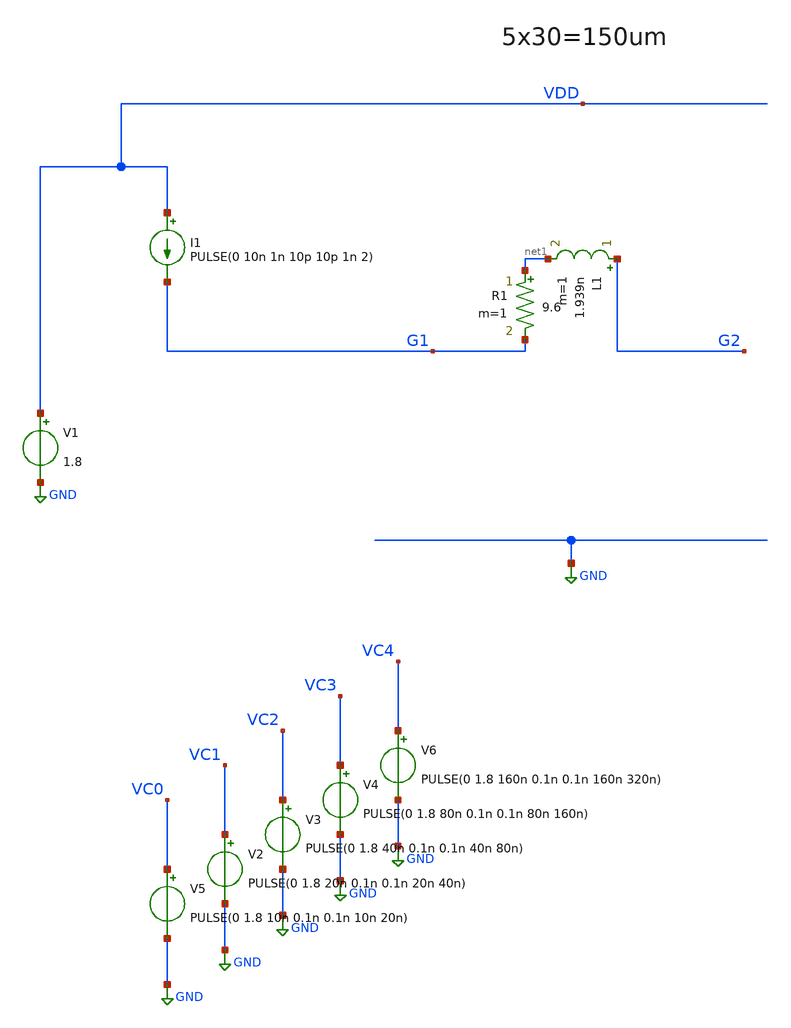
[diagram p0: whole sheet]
** sch_path: xschem/OSC_LF1_PEX.sch
**.subckt OSC_LF1_PEX
V1 VDD GND 1.8
I1 VDD G1 PULSE(0 10n 1n 10p 10p 1n 2)
L1 G2 net1 1.939n m=1
V5 VC0 GND PULSE(0 1.8 10n 0.1n 0.1n 10n 20n)
V2 VC1 GND PULSE(0 1.8 20n 0.1n 0.1n 20n 40n)
V3 VC2 GND PULSE(0 1.8 40n 0.1n 0.1n 40n 80n)
V4 VC3 GND PULSE(0 1.8 80n 0.1n 0.1n 80n 160n)
V6 VC4 GND PULSE(0 1.8 160n 0.1n 0.1n 160n 320n)
R1 net1 G1 9.6 m=1
**** begin user architecture code
.lib $::SKYWATER_MODELS/sky130.lib.spice ff
* .include $::PDKPATH/libs.ref/sky130_fd_sc_hvl/spice/sky130_fd_sc_hvl.spice



* .subckt sky130_fd_pr__rf_nfet_01v8_bM04W5p00L0p15_ext DRAIN GATE SOURCE SUBSTRATE
* X0 DRAIN GATE SOURCE SUBSTRATE sky130_fd_pr__nfet_01v8 ad=2.828e+12p pd=2.132e+07u as=4.242e+12p
*+ ps=3.198e+07u w=5.05e+06u l=150000u
* X1 SOURCE SUBSTRATE SUBSTRATE SUBSTRATE sky130_fd_pr__nfet_01v8 ad=0p pd=0u as=3.03e+12p
*+ ps=2.14e+07u w=5.05e+06u l=150000u
* X2 SOURCE GATE DRAIN SUBSTRATE sky130_fd_pr__nfet_01v8 ad=0p pd=0u as=0p ps=0u w=5.05e+06u
*+ l=150000u
* X3 DRAIN GATE SOURCE SUBSTRATE sky130_fd_pr__nfet_01v8 ad=0p pd=0u as=0p ps=0u w=5.05e+06u
*+ l=150000u
* X4 SUBSTRATE SUBSTRATE SOURCE SUBSTRATE sky130_fd_pr__nfet_01v8 ad=0p pd=0u as=0p ps=0u
*+ w=5.05e+06u l=150000u
* X5 SOURCE GATE DRAIN SUBSTRATE sky130_fd_pr__nfet_01v8 ad=0p pd=0u as=0p ps=0u w=5.05e+06u
*+ l=150000u
* .ends

**** CROSS COUPLED PAIRS ****

.subckt XCP VH VL G1 G2

.subckt sky130_fd_pr__rf_pfet_01v8_aF04W5p00L0p15 DRAIN GATE SOURCE
X0 DRAIN GATE SOURCE SOURCE sky130_fd_pr__pfet_01v8 ad=2.8e+12p pd=2.112e+07u as=4.05e+12p
+ ps=3.162e+07u w=5e+06u l=150000u
X1 SOURCE GATE DRAIN SOURCE sky130_fd_pr__pfet_01v8 ad=0p pd=0u as=0p ps=0u w=5e+06u l=150000u
X2 SOURCE GATE DRAIN SOURCE sky130_fd_pr__pfet_01v8 ad=0p pd=0u as=0p ps=0u w=5e+06u l=150000u
X3 DRAIN GATE SOURCE SOURCE sky130_fd_pr__pfet_01v8 ad=0p pd=0u as=0p ps=0u w=5e+06u l=150000u
C0 DRAIN SOURCE 6.07fF
.ends



X0 VL G1 G2 VL sky130_fd_pr__nfet_01v8 ad=0p pd=0u as=0p ps=0u w=5.05e+06u l=150000u
X1 VL G1 G2 VL sky130_fd_pr__nfet_01v8 ad=0p pd=0u as=0p ps=0u w=5.05e+06u l=150000u
X2 G2 G1 VL VL sky130_fd_pr__nfet_01v8 ad=0p pd=0u as=0p ps=0u w=5.05e+06u l=150000u
X3 G2 G1 VL VL sky130_fd_pr__nfet_01v8 ad=0p pd=0u as=0p ps=0u w=5.05e+06u l=150000u
X4 VL G1 G2 VL sky130_fd_pr__nfet_01v8 ad=0p pd=0u as=0p ps=0u w=5.05e+06u l=150000u
X5 VL G1 G2 VL sky130_fd_pr__nfet_01v8 ad=0p pd=0u as=0p ps=0u w=5.05e+06u l=150000u
X6 G2 G1 VL VL sky130_fd_pr__nfet_01v8 ad=0p pd=0u as=0p ps=0u w=5.05e+06u l=150000u
X7 G2 G1 VL VL sky130_fd_pr__nfet_01v8 ad=0p pd=0u as=0p ps=0u w=5.05e+06u l=150000u
X8 VL G1 G2 VL sky130_fd_pr__nfet_01v8 ad=0p pd=0u as=0p ps=0u w=5.05e+06u l=150000u
X9 VL G1 G2 VL sky130_fd_pr__nfet_01v8 ad=0p pd=0u as=0p ps=0u w=5.05e+06u l=150000u
X10 G2 G1 VL VL sky130_fd_pr__nfet_01v8 ad=0p pd=0u as=0p ps=0u w=5.05e+06u l=150000u
X11 G2 G1 VL VL sky130_fd_pr__nfet_01v8 ad=0p pd=0u as=0p ps=0u w=5.05e+06u l=150000u
X12 VL G2 G1 VL sky130_fd_pr__nfet_01v8 ad=0p pd=0u as=0p ps=0u w=5.05e+06u l=150000u
X13 VL G2 G1 VL sky130_fd_pr__nfet_01v8 ad=0p pd=0u as=0p ps=0u w=5.05e+06u l=150000u
X14 G1 G2 VL VL sky130_fd_pr__nfet_01v8 ad=0p pd=0u as=0p ps=0u w=5.05e+06u l=150000u
X15 G1 G2 VL VL sky130_fd_pr__nfet_01v8 ad=0p pd=0u as=0p ps=0u w=5.05e+06u l=150000u
X16 VL G2 G1 VL sky130_fd_pr__nfet_01v8 ad=0p pd=0u as=0p ps=0u w=5.05e+06u l=150000u
X17 VL G2 G1 VL sky130_fd_pr__nfet_01v8 ad=0p pd=0u as=0p ps=0u w=5.05e+06u l=150000u
X18 G1 G2 VL VL sky130_fd_pr__nfet_01v8 ad=0p pd=0u as=0p ps=0u w=5.05e+06u l=150000u
X19 G1 G2 VL VL sky130_fd_pr__nfet_01v8 ad=0p pd=0u as=0p ps=0u w=5.05e+06u l=150000u
X20 VL G2 G1 VL sky130_fd_pr__nfet_01v8 ad=0p pd=0u as=0p ps=0u w=5.05e+06u l=150000u
X21 VL G2 G1 VL sky130_fd_pr__nfet_01v8 ad=0p pd=0u as=0p ps=0u w=5.05e+06u l=150000u
X22 G1 G2 VL VL sky130_fd_pr__nfet_01v8 ad=0p pd=0u as=0p ps=0u w=5.05e+06u l=150000u
X23 G1 G2 VL VL sky130_fd_pr__nfet_01v8 ad=0p pd=0u as=0p ps=0u w=5.05e+06u l=150000u
C0 G1 VH 48.54fF
C1 VH G2 48.59fF
C2 G1 G2 16.60fF
XRF_pfet_28xW5p0L0p15_0/sky130_fd_pr__rf_pfet_01v8_aF04W5p00L0p15_0 G2 G1 VH
+ sky130_fd_pr__rf_pfet_01v8_aF04W5p00L0p15
XRF_pfet_28xW5p0L0p15_0/sky130_fd_pr__rf_pfet_01v8_aF04W5p00L0p15_1 G2 G1 VH
+ sky130_fd_pr__rf_pfet_01v8_aF04W5p00L0p15
XRF_pfet_28xW5p0L0p15_0/sky130_fd_pr__rf_pfet_01v8_aF04W5p00L0p15_2 G2 G1 VH
+ sky130_fd_pr__rf_pfet_01v8_aF04W5p00L0p15
XRF_pfet_28xW5p0L0p15_0/sky130_fd_pr__rf_pfet_01v8_aF04W5p00L0p15_3 G2 G1 VH
+ sky130_fd_pr__rf_pfet_01v8_aF04W5p00L0p15
XRF_pfet_28xW5p0L0p15_0/sky130_fd_pr__rf_pfet_01v8_aF04W5p00L0p15_4 G2 G1 VH
+ sky130_fd_pr__rf_pfet_01v8_aF04W5p00L0p15
XRF_pfet_28xW5p0L0p15_0/sky130_fd_pr__rf_pfet_01v8_aF04W5p00L0p15_5 G2 G1 VH
+ sky130_fd_pr__rf_pfet_01v8_aF04W5p00L0p15
XRF_pfet_28xW5p0L0p15_0/sky130_fd_pr__rf_pfet_01v8_aF04W5p00L0p15_6 G2 G1 VH
+ sky130_fd_pr__rf_pfet_01v8_aF04W5p00L0p15
XRF_pfet_28xW5p0L0p15_1/sky130_fd_pr__rf_pfet_01v8_aF04W5p00L0p15_0 G1 G2 VH
+ sky130_fd_pr__rf_pfet_01v8_aF04W5p00L0p15
XRF_pfet_28xW5p0L0p15_1/sky130_fd_pr__rf_pfet_01v8_aF04W5p00L0p15_1 G1 G2 VH
+ sky130_fd_pr__rf_pfet_01v8_aF04W5p00L0p15
XRF_pfet_28xW5p0L0p15_1/sky130_fd_pr__rf_pfet_01v8_aF04W5p00L0p15_2 G1 G2 VH
+ sky130_fd_pr__rf_pfet_01v8_aF04W5p00L0p15
XRF_pfet_28xW5p0L0p15_1/sky130_fd_pr__rf_pfet_01v8_aF04W5p00L0p15_3 G1 G2 VH
+ sky130_fd_pr__rf_pfet_01v8_aF04W5p00L0p15
XRF_pfet_28xW5p0L0p15_1/sky130_fd_pr__rf_pfet_01v8_aF04W5p00L0p15_4 G1 G2 VH
+ sky130_fd_pr__rf_pfet_01v8_aF04W5p00L0p15
XRF_pfet_28xW5p0L0p15_1/sky130_fd_pr__rf_pfet_01v8_aF04W5p00L0p15_5 G1 G2 VH
+ sky130_fd_pr__rf_pfet_01v8_aF04W5p00L0p15
XRF_pfet_28xW5p0L0p15_1/sky130_fd_pr__rf_pfet_01v8_aF04W5p00L0p15_6 G1 G2 VH
+ sky130_fd_pr__rf_pfet_01v8_aF04W5p00L0p15
C3 G1 VL 22.49fF
C4 G2 VL 22.37fF
C5 VH VL 25.01fF
.ends


**** CAPTUNE ****

.subckt CAPTUNE TOP BOT SUB G0 G1 G2 G3 G4

X0 BOT G0 sky130_fd_pr__rf_nfet_01v8_aM04W5p00L0p15_fingered_0/S SUB sky130_fd_pr__nfet_01v8 ad=0p
+ pd=0u as=0p ps=0u w=5.05e+06u l=150000u
X1 BOT G0 sky130_fd_pr__rf_nfet_01v8_aM04W5p00L0p15_fingered_0/S SUB sky130_fd_pr__nfet_01v8 ad=0p
+ pd=0u as=0p ps=0u w=5.05e+06u l=150000u
X2 sky130_fd_pr__rf_nfet_01v8_aM04W5p00L0p15_fingered_0/S G0 BOT SUB sky130_fd_pr__nfet_01v8 ad=0p
+ pd=0u as=0p ps=0u w=5.05e+06u l=150000u
X3 sky130_fd_pr__rf_nfet_01v8_aM04W5p00L0p15_fingered_0/S G0 BOT SUB sky130_fd_pr__nfet_01v8 ad=0p
+ pd=0u as=0p ps=0u w=5.05e+06u l=150000u
X4 BOT G1 sky130_fd_pr__rf_nfet_01v8_aM04W5p00L0p15_fingered_1/S SUB sky130_fd_pr__nfet_01v8 ad=0p
+ pd=0u as=0p ps=0u w=5.05e+06u l=150000u
X5 BOT G1 sky130_fd_pr__rf_nfet_01v8_aM04W5p00L0p15_fingered_1/S SUB sky130_fd_pr__nfet_01v8 ad=0p
+ pd=0u as=0p ps=0u w=5.05e+06u l=150000u
X6 sky130_fd_pr__rf_nfet_01v8_aM04W5p00L0p15_fingered_1/S G1 BOT SUB sky130_fd_pr__nfet_01v8 ad=0p
+ pd=0u as=0p ps=0u w=5.05e+06u l=150000u
X7 sky130_fd_pr__rf_nfet_01v8_aM04W5p00L0p15_fingered_1/S G1 BOT SUB sky130_fd_pr__nfet_01v8 ad=0p
+ pd=0u as=0p ps=0u w=5.05e+06u l=150000u
X8 BOT G2 sky130_fd_pr__rf_nfet_01v8_aM04W5p00L0p15_fingered_2/S SUB sky130_fd_pr__nfet_01v8 ad=0p
+ pd=0u as=0p ps=0u w=5.05e+06u l=150000u
X9 BOT G2 sky130_fd_pr__rf_nfet_01v8_aM04W5p00L0p15_fingered_2/S SUB sky130_fd_pr__nfet_01v8 ad=0p
+ pd=0u as=0p ps=0u w=5.05e+06u l=150000u
X10 sky130_fd_pr__rf_nfet_01v8_aM04W5p00L0p15_fingered_2/S G2 BOT SUB sky130_fd_pr__nfet_01v8 ad=0p
+ pd=0u as=0p ps=0u w=5.05e+06u l=150000u
X11 sky130_fd_pr__rf_nfet_01v8_aM04W5p00L0p15_fingered_2/S G2 BOT SUB sky130_fd_pr__nfet_01v8 ad=0p
+ pd=0u as=0p ps=0u w=5.05e+06u l=150000u
X12 BOT G3 sky130_fd_pr__rf_nfet_01v8_aM04W5p00L0p15_fingered_4/S SUB sky130_fd_pr__nfet_01v8 ad=0p
+ pd=0u as=0p ps=0u w=5.05e+06u l=150000u
X13 BOT G3 sky130_fd_pr__rf_nfet_01v8_aM04W5p00L0p15_fingered_4/S SUB sky130_fd_pr__nfet_01v8 ad=0p
+ pd=0u as=0p ps=0u w=5.05e+06u l=150000u
X14 sky130_fd_pr__rf_nfet_01v8_aM04W5p00L0p15_fingered_4/S G3 BOT SUB sky130_fd_pr__nfet_01v8 ad=0p
+ pd=0u as=0p ps=0u w=5.05e+06u l=150000u
X15 sky130_fd_pr__rf_nfet_01v8_aM04W5p00L0p15_fingered_4/S G3 BOT SUB sky130_fd_pr__nfet_01v8 ad=0p
+ pd=0u as=0p ps=0u w=5.05e+06u l=150000u
X16 BOT G3 sky130_fd_pr__rf_nfet_01v8_aM04W5p00L0p15_fingered_4/S SUB sky130_fd_pr__nfet_01v8 ad=0p
+ pd=0u as=0p ps=0u w=5.05e+06u l=150000u
X17 BOT G3 sky130_fd_pr__rf_nfet_01v8_aM04W5p00L0p15_fingered_4/S SUB sky130_fd_pr__nfet_01v8 ad=0p
+ pd=0u as=0p ps=0u w=5.05e+06u l=150000u
X18 sky130_fd_pr__rf_nfet_01v8_aM04W5p00L0p15_fingered_4/S G3 BOT SUB sky130_fd_pr__nfet_01v8 ad=0p
+ pd=0u as=0p ps=0u w=5.05e+06u l=150000u
X19 sky130_fd_pr__rf_nfet_01v8_aM04W5p00L0p15_fingered_4/S G3 BOT SUB sky130_fd_pr__nfet_01v8 ad=0p
+ pd=0u as=0p ps=0u w=5.05e+06u l=150000u
X20 BOT G4 sky130_fd_pr__rf_nfet_01v8_aM04W5p00L0p15_fingered_6/S SUB sky130_fd_pr__nfet_01v8 ad=0p
+ pd=0u as=0p ps=0u w=5.05e+06u l=150000u
X21 BOT G4 sky130_fd_pr__rf_nfet_01v8_aM04W5p00L0p15_fingered_6/S SUB sky130_fd_pr__nfet_01v8 ad=0p
+ pd=0u as=0p ps=0u w=5.05e+06u l=150000u
X22 sky130_fd_pr__rf_nfet_01v8_aM04W5p00L0p15_fingered_6/S G4 BOT SUB sky130_fd_pr__nfet_01v8 ad=0p
+ pd=0u as=0p ps=0u w=5.05e+06u l=150000u
X23 sky130_fd_pr__rf_nfet_01v8_aM04W5p00L0p15_fingered_6/S G4 BOT SUB sky130_fd_pr__nfet_01v8 ad=0p
+ pd=0u as=0p ps=0u w=5.05e+06u l=150000u
X24 BOT G4 sky130_fd_pr__rf_nfet_01v8_aM04W5p00L0p15_fingered_6/S SUB sky130_fd_pr__nfet_01v8 ad=0p
+ pd=0u as=0p ps=0u w=5.05e+06u l=150000u
X25 BOT G4 sky130_fd_pr__rf_nfet_01v8_aM04W5p00L0p15_fingered_6/S SUB sky130_fd_pr__nfet_01v8 ad=0p
+ pd=0u as=0p ps=0u w=5.05e+06u l=150000u
X26 sky130_fd_pr__rf_nfet_01v8_aM04W5p00L0p15_fingered_6/S G4 BOT SUB sky130_fd_pr__nfet_01v8 ad=0p
+ pd=0u as=0p ps=0u w=5.05e+06u l=150000u
X27 sky130_fd_pr__rf_nfet_01v8_aM04W5p00L0p15_fingered_6/S G4 BOT SUB sky130_fd_pr__nfet_01v8 ad=0p
+ pd=0u as=0p ps=0u w=5.05e+06u l=150000u
X28 TOP sky130_fd_pr__rf_nfet_01v8_aM04W5p00L0p15_fingered_4/S sky130_fd_pr__cap_mim_m3_1 l=4e+06u
+ w=1e+07u
X29 TOP sky130_fd_pr__rf_nfet_01v8_aM04W5p00L0p15_fingered_0/S sky130_fd_pr__cap_mim_m3_1 l=1e+06u
+ w=5e+06u
X30 TOP sky130_fd_pr__rf_nfet_01v8_aM04W5p00L0p15_fingered_6/S sky130_fd_pr__cap_mim_m3_1 l=8e+06u
+ w=1e+07u
X31 TOP sky130_fd_pr__rf_nfet_01v8_aM04W5p00L0p15_fingered_1/S sky130_fd_pr__cap_mim_m3_1 l=1e+06u
+ w=1e+07u
X32 TOP sky130_fd_pr__rf_nfet_01v8_aM04W5p00L0p15_fingered_2/S sky130_fd_pr__cap_mim_m3_1 l=2e+06u
+ w=1e+07u
C0 TOP sky130_fd_pr__rf_nfet_01v8_aM04W5p00L0p15_fingered_4/S 4.41fF
C1 TOP sky130_fd_pr__rf_nfet_01v8_aM04W5p00L0p15_fingered_2/S 2.57fF
C2 BOT sky130_fd_pr__rf_nfet_01v8_aM04W5p00L0p15_fingered_1/S 10.32fF
C3 sky130_fd_pr__rf_nfet_01v8_aM04W5p00L0p15_fingered_4/S BOT 20.62fF
C4 BOT sky130_fd_pr__rf_nfet_01v8_aM04W5p00L0p15_fingered_2/S 10.36fF
C5 sky130_fd_pr__rf_nfet_01v8_aM04W5p00L0p15_fingered_0/S BOT 10.34fF
C6 sky130_fd_pr__rf_nfet_01v8_aM04W5p00L0p15_fingered_6/S TOP 8.02fF
C7 BOT G4 2.52fF
C8 BOT G3 2.53fF
C9 sky130_fd_pr__rf_nfet_01v8_aM04W5p00L0p15_fingered_6/S BOT 20.72fF
C10 TOP SUB 3.06fF
C11 sky130_fd_pr__rf_nfet_01v8_aM04W5p00L0p15_fingered_6/S SUB 2.81fF
C12 G4 SUB 3.15fF
C13 BOT SUB 17.11fF
C14 G3 SUB 3.15fF

.ends




**** COMPLETE *****

.subckt COMPLETE VH VL I1 I2 G0 G1 G2 G3 G4

.subckt sky130_fd_pr__rf_pfet_01v8_aF04W5p00L0p15 DRAIN GATE SOURCE
X0 DRAIN GATE SOURCE SOURCE sky130_fd_pr__pfet_01v8 ad=2.8e+12p pd=2.112e+07u as=4.05e+12p
+ ps=3.162e+07u w=5e+06u l=150000u
X1 SOURCE GATE DRAIN SOURCE sky130_fd_pr__pfet_01v8 ad=0p pd=0u as=0p ps=0u w=5e+06u l=150000u
X2 SOURCE GATE DRAIN SOURCE sky130_fd_pr__pfet_01v8 ad=0p pd=0u as=0p ps=0u w=5e+06u l=150000u
X3 DRAIN GATE SOURCE SOURCE sky130_fd_pr__pfet_01v8 ad=0p pd=0u as=0p ps=0u w=5e+06u l=150000u
C0 DRAIN SOURCE 6.07fF
.ends

X0 I2 G0 captuner_complete_2_0/sky130_fd_pr__rf_nfet_01v8_aM04W5p00L0p15_fingered_0/S VL
+ sky130_fd_pr__nfet_01v8 ad=0p pd=0u as=0p ps=0u w=5.05e+06u l=150000u
X1 I2 G0 captuner_complete_2_0/sky130_fd_pr__rf_nfet_01v8_aM04W5p00L0p15_fingered_0/S VL
+ sky130_fd_pr__nfet_01v8 ad=0p pd=0u as=0p ps=0u w=5.05e+06u l=150000u
X2 captuner_complete_2_0/sky130_fd_pr__rf_nfet_01v8_aM04W5p00L0p15_fingered_0/S G0 I2 VL
+ sky130_fd_pr__nfet_01v8 ad=0p pd=0u as=0p ps=0u w=5.05e+06u l=150000u
X3 captuner_complete_2_0/sky130_fd_pr__rf_nfet_01v8_aM04W5p00L0p15_fingered_0/S G0 I2 VL
+ sky130_fd_pr__nfet_01v8 ad=0p pd=0u as=0p ps=0u w=5.05e+06u l=150000u
X4 I2 G1 captuner_complete_2_0/sky130_fd_pr__rf_nfet_01v8_aM04W5p00L0p15_fingered_1/S VL
+ sky130_fd_pr__nfet_01v8 ad=0p pd=0u as=0p ps=0u w=5.05e+06u l=150000u
X5 I2 G1 captuner_complete_2_0/sky130_fd_pr__rf_nfet_01v8_aM04W5p00L0p15_fingered_1/S VL
+ sky130_fd_pr__nfet_01v8 ad=0p pd=0u as=0p ps=0u w=5.05e+06u l=150000u
X6 captuner_complete_2_0/sky130_fd_pr__rf_nfet_01v8_aM04W5p00L0p15_fingered_1/S G1 I2 VL
+ sky130_fd_pr__nfet_01v8 ad=0p pd=0u as=0p ps=0u w=5.05e+06u l=150000u
X7 captuner_complete_2_0/sky130_fd_pr__rf_nfet_01v8_aM04W5p00L0p15_fingered_1/S G1 I2 VL
+ sky130_fd_pr__nfet_01v8 ad=0p pd=0u as=0p ps=0u w=5.05e+06u l=150000u
X8 I2 G2 captuner_complete_2_0/sky130_fd_pr__rf_nfet_01v8_aM04W5p00L0p15_fingered_2/S VL
+ sky130_fd_pr__nfet_01v8 ad=0p pd=0u as=0p ps=0u w=5.05e+06u l=150000u
X9 I2 G2 captuner_complete_2_0/sky130_fd_pr__rf_nfet_01v8_aM04W5p00L0p15_fingered_2/S VL
+ sky130_fd_pr__nfet_01v8 ad=0p pd=0u as=0p ps=0u w=5.05e+06u l=150000u
X10 captuner_complete_2_0/sky130_fd_pr__rf_nfet_01v8_aM04W5p00L0p15_fingered_2/S G2 I2 VL
+ sky130_fd_pr__nfet_01v8 ad=0p pd=0u as=0p ps=0u w=5.05e+06u l=150000u
X11 captuner_complete_2_0/sky130_fd_pr__rf_nfet_01v8_aM04W5p00L0p15_fingered_2/S G2 I2 VL
+ sky130_fd_pr__nfet_01v8 ad=0p pd=0u as=0p ps=0u w=5.05e+06u l=150000u
X12 I2 G3 captuner_complete_2_0/sky130_fd_pr__rf_nfet_01v8_aM04W5p00L0p15_fingered_4/S VL
+ sky130_fd_pr__nfet_01v8 ad=0p pd=0u as=0p ps=0u w=5.05e+06u l=150000u
X13 I2 G3 captuner_complete_2_0/sky130_fd_pr__rf_nfet_01v8_aM04W5p00L0p15_fingered_4/S VL
+ sky130_fd_pr__nfet_01v8 ad=0p pd=0u as=0p ps=0u w=5.05e+06u l=150000u
X14 captuner_complete_2_0/sky130_fd_pr__rf_nfet_01v8_aM04W5p00L0p15_fingered_4/S G3 I2 VL
+ sky130_fd_pr__nfet_01v8 ad=0p pd=0u as=0p ps=0u w=5.05e+06u l=150000u
X15 captuner_complete_2_0/sky130_fd_pr__rf_nfet_01v8_aM04W5p00L0p15_fingered_4/S G3 I2 VL
+ sky130_fd_pr__nfet_01v8 ad=0p pd=0u as=0p ps=0u w=5.05e+06u l=150000u
X16 I2 G3 captuner_complete_2_0/sky130_fd_pr__rf_nfet_01v8_aM04W5p00L0p15_fingered_4/S VL
+ sky130_fd_pr__nfet_01v8 ad=0p pd=0u as=0p ps=0u w=5.05e+06u l=150000u
X17 I2 G3 captuner_complete_2_0/sky130_fd_pr__rf_nfet_01v8_aM04W5p00L0p15_fingered_4/S VL
+ sky130_fd_pr__nfet_01v8 ad=0p pd=0u as=0p ps=0u w=5.05e+06u l=150000u
X18 captuner_complete_2_0/sky130_fd_pr__rf_nfet_01v8_aM04W5p00L0p15_fingered_4/S G3 I2 VL
+ sky130_fd_pr__nfet_01v8 ad=0p pd=0u as=0p ps=0u w=5.05e+06u l=150000u
X19 captuner_complete_2_0/sky130_fd_pr__rf_nfet_01v8_aM04W5p00L0p15_fingered_4/S G3 I2 VL
+ sky130_fd_pr__nfet_01v8 ad=0p pd=0u as=0p ps=0u w=5.05e+06u l=150000u
X20 I2 G4 captuner_complete_2_0/sky130_fd_pr__rf_nfet_01v8_aM04W5p00L0p15_fingered_6/S VL
+ sky130_fd_pr__nfet_01v8 ad=0p pd=0u as=0p ps=0u w=5.05e+06u l=150000u
X21 I2 G4 captuner_complete_2_0/sky130_fd_pr__rf_nfet_01v8_aM04W5p00L0p15_fingered_6/S VL
+ sky130_fd_pr__nfet_01v8 ad=0p pd=0u as=0p ps=0u w=5.05e+06u l=150000u
X22 captuner_complete_2_0/sky130_fd_pr__rf_nfet_01v8_aM04W5p00L0p15_fingered_6/S G4 I2 VL
+ sky130_fd_pr__nfet_01v8 ad=0p pd=0u as=0p ps=0u w=5.05e+06u l=150000u
X23 captuner_complete_2_0/sky130_fd_pr__rf_nfet_01v8_aM04W5p00L0p15_fingered_6/S G4 I2 VL
+ sky130_fd_pr__nfet_01v8 ad=0p pd=0u as=0p ps=0u w=5.05e+06u l=150000u
X24 I2 G4 captuner_complete_2_0/sky130_fd_pr__rf_nfet_01v8_aM04W5p00L0p15_fingered_6/S VL
+ sky130_fd_pr__nfet_01v8 ad=0p pd=0u as=0p ps=0u w=5.05e+06u l=150000u
X25 I2 G4 captuner_complete_2_0/sky130_fd_pr__rf_nfet_01v8_aM04W5p00L0p15_fingered_6/S VL
+ sky130_fd_pr__nfet_01v8 ad=0p pd=0u as=0p ps=0u w=5.05e+06u l=150000u
X26 captuner_complete_2_0/sky130_fd_pr__rf_nfet_01v8_aM04W5p00L0p15_fingered_6/S G4 I2 VL
+ sky130_fd_pr__nfet_01v8 ad=0p pd=0u as=0p ps=0u w=5.05e+06u l=150000u
X27 captuner_complete_2_0/sky130_fd_pr__rf_nfet_01v8_aM04W5p00L0p15_fingered_6/S G4 I2 VL
+ sky130_fd_pr__nfet_01v8 ad=0p pd=0u as=0p ps=0u w=5.05e+06u l=150000u
X28 I1 captuner_complete_2_0/sky130_fd_pr__rf_nfet_01v8_aM04W5p00L0p15_fingered_4/S
+ sky130_fd_pr__cap_mim_m3_1 l=4e+06u w=1e+07u
X29 I1 captuner_complete_2_0/sky130_fd_pr__rf_nfet_01v8_aM04W5p00L0p15_fingered_0/S
+ sky130_fd_pr__cap_mim_m3_1 l=1e+06u w=5e+06u
X30 I1 captuner_complete_2_0/sky130_fd_pr__rf_nfet_01v8_aM04W5p00L0p15_fingered_6/S
+ sky130_fd_pr__cap_mim_m3_1 l=8e+06u w=1e+07u
X31 I1 captuner_complete_2_0/sky130_fd_pr__rf_nfet_01v8_aM04W5p00L0p15_fingered_1/S
+ sky130_fd_pr__cap_mim_m3_1 l=1e+06u w=1e+07u
X32 I1 captuner_complete_2_0/sky130_fd_pr__rf_nfet_01v8_aM04W5p00L0p15_fingered_2/S
+ sky130_fd_pr__cap_mim_m3_1 l=2e+06u w=1e+07u
X33 VL I1 I2 VL sky130_fd_pr__nfet_01v8 ad=0p pd=0u as=0p ps=0u w=5.05e+06u l=150000u
X34 VL I1 I2 VL sky130_fd_pr__nfet_01v8 ad=0p pd=0u as=0p ps=0u w=5.05e+06u l=150000u
X35 I2 I1 VL VL sky130_fd_pr__nfet_01v8 ad=0p pd=0u as=0p ps=0u w=5.05e+06u l=150000u
X36 I2 I1 VL VL sky130_fd_pr__nfet_01v8 ad=0p pd=0u as=0p ps=0u w=5.05e+06u l=150000u
X37 VL I1 I2 VL sky130_fd_pr__nfet_01v8 ad=0p pd=0u as=0p ps=0u w=5.05e+06u l=150000u
X38 VL I1 I2 VL sky130_fd_pr__nfet_01v8 ad=0p pd=0u as=0p ps=0u w=5.05e+06u l=150000u
X39 I2 I1 VL VL sky130_fd_pr__nfet_01v8 ad=0p pd=0u as=0p ps=0u w=5.05e+06u l=150000u
X40 I2 I1 VL VL sky130_fd_pr__nfet_01v8 ad=0p pd=0u as=0p ps=0u w=5.05e+06u l=150000u
X41 VL I1 I2 VL sky130_fd_pr__nfet_01v8 ad=0p pd=0u as=0p ps=0u w=5.05e+06u l=150000u
X42 VL I1 I2 VL sky130_fd_pr__nfet_01v8 ad=0p pd=0u as=0p ps=0u w=5.05e+06u l=150000u
X43 I2 I1 VL VL sky130_fd_pr__nfet_01v8 ad=0p pd=0u as=0p ps=0u w=5.05e+06u l=150000u
X44 I2 I1 VL VL sky130_fd_pr__nfet_01v8 ad=0p pd=0u as=0p ps=0u w=5.05e+06u l=150000u
X45 VL I2 I1 VL sky130_fd_pr__nfet_01v8 ad=0p pd=0u as=0p ps=0u w=5.05e+06u l=150000u
X46 VL I2 I1 VL sky130_fd_pr__nfet_01v8 ad=0p pd=0u as=0p ps=0u w=5.05e+06u l=150000u
X47 I1 I2 VL VL sky130_fd_pr__nfet_01v8 ad=0p pd=0u as=0p ps=0u w=5.05e+06u l=150000u
X48 I1 I2 VL VL sky130_fd_pr__nfet_01v8 ad=0p pd=0u as=0p ps=0u w=5.05e+06u l=150000u
X49 VL I2 I1 VL sky130_fd_pr__nfet_01v8 ad=0p pd=0u as=0p ps=0u w=5.05e+06u l=150000u
X50 VL I2 I1 VL sky130_fd_pr__nfet_01v8 ad=0p pd=0u as=0p ps=0u w=5.05e+06u l=150000u
X51 I1 I2 VL VL sky130_fd_pr__nfet_01v8 ad=0p pd=0u as=0p ps=0u w=5.05e+06u l=150000u
X52 I1 I2 VL VL sky130_fd_pr__nfet_01v8 ad=0p pd=0u as=0p ps=0u w=5.05e+06u l=150000u
X53 VL I2 I1 VL sky130_fd_pr__nfet_01v8 ad=0p pd=0u as=0p ps=0u w=5.05e+06u l=150000u
X54 VL I2 I1 VL sky130_fd_pr__nfet_01v8 ad=0p pd=0u as=0p ps=0u w=5.05e+06u l=150000u
X55 I1 I2 VL VL sky130_fd_pr__nfet_01v8 ad=0p pd=0u as=0p ps=0u w=5.05e+06u l=150000u
X56 I1 I2 VL VL sky130_fd_pr__nfet_01v8 ad=0p pd=0u as=0p ps=0u w=5.05e+06u l=150000u
C0 captuner_complete_2_0/sky130_fd_pr__rf_nfet_01v8_aM04W5p00L0p15_fingered_2/S I2 10.36fF
C1 captuner_complete_2_0/sky130_fd_pr__rf_nfet_01v8_aM04W5p00L0p15_fingered_2/S I1 2.57fF
C2 I2 captuner_complete_2_0/sky130_fd_pr__rf_nfet_01v8_aM04W5p00L0p15_fingered_4/S 20.62fF
C3 I1 captuner_complete_2_0/sky130_fd_pr__rf_nfet_01v8_aM04W5p00L0p15_fingered_4/S 4.41fF
C4 G4 I2 2.69fF
C5 captuner_complete_2_0/sky130_fd_pr__rf_nfet_01v8_aM04W5p00L0p15_fingered_0/S I2 10.35fF
C6 I2 captuner_complete_2_0/sky130_fd_pr__rf_nfet_01v8_aM04W5p00L0p15_fingered_6/S 21.16fF
C7 captuner_complete_2_0/sky130_fd_pr__rf_nfet_01v8_aM04W5p00L0p15_fingered_1/S I2 10.32fF
C8 I1 captuner_complete_2_0/sky130_fd_pr__rf_nfet_01v8_aM04W5p00L0p15_fingered_6/S 8.73fF
C9 VH I2 56.20fF
C10 VH I1 56.69fF
C11 I2 I1 20.88fF
C12 I2 G3 2.54fF
Xsky130_fd_pr__cap_vpp_08p6x07p8_m1m2m3_shieldl1_0 VL VH VL
+ sky130_fd_pr__cap_vpp_08p6x07p8_m1m2m3_shieldl1
Xsky130_fd_pr__cap_vpp_08p6x07p8_m1m2m3_shieldl1_1 VL VH VL
+ sky130_fd_pr__cap_vpp_08p6x07p8_m1m2m3_shieldl1
Xsky130_fd_pr__cap_vpp_08p6x07p8_m1m2m3_shieldl1_2 VL VH VL
+ sky130_fd_pr__cap_vpp_08p6x07p8_m1m2m3_shieldl1
XXCP_1_0/RF_pfet_28xW5p0L0p15_0/sky130_fd_pr__rf_pfet_01v8_aF04W5p00L0p15_0 I2 I1  VH
+ sky130_fd_pr__rf_pfet_01v8_aF04W5p00L0p15
XXCP_1_0/RF_pfet_28xW5p0L0p15_0/sky130_fd_pr__rf_pfet_01v8_aF04W5p00L0p15_1 I2 I1  VH
+ sky130_fd_pr__rf_pfet_01v8_aF04W5p00L0p15
XXCP_1_0/RF_pfet_28xW5p0L0p15_0/sky130_fd_pr__rf_pfet_01v8_aF04W5p00L0p15_2 I2 I1  VH
+ sky130_fd_pr__rf_pfet_01v8_aF04W5p00L0p15
XXCP_1_0/RF_pfet_28xW5p0L0p15_0/sky130_fd_pr__rf_pfet_01v8_aF04W5p00L0p15_3 I2 I1  VH
+ sky130_fd_pr__rf_pfet_01v8_aF04W5p00L0p15
XXCP_1_0/RF_pfet_28xW5p0L0p15_0/sky130_fd_pr__rf_pfet_01v8_aF04W5p00L0p15_4 I2 I1  VH
+ sky130_fd_pr__rf_pfet_01v8_aF04W5p00L0p15
XXCP_1_0/RF_pfet_28xW5p0L0p15_0/sky130_fd_pr__rf_pfet_01v8_aF04W5p00L0p15_5 I2 I1  VH
+ sky130_fd_pr__rf_pfet_01v8_aF04W5p00L0p15
XXCP_1_0/RF_pfet_28xW5p0L0p15_0/sky130_fd_pr__rf_pfet_01v8_aF04W5p00L0p15_6 I2 I1  VH
+ sky130_fd_pr__rf_pfet_01v8_aF04W5p00L0p15
XXCP_1_0/RF_pfet_28xW5p0L0p15_1/sky130_fd_pr__rf_pfet_01v8_aF04W5p00L0p15_0 I1 I2  VH
+ sky130_fd_pr__rf_pfet_01v8_aF04W5p00L0p15
XXCP_1_0/RF_pfet_28xW5p0L0p15_1/sky130_fd_pr__rf_pfet_01v8_aF04W5p00L0p15_1 I1 I2  VH
+ sky130_fd_pr__rf_pfet_01v8_aF04W5p00L0p15
XXCP_1_0/RF_pfet_28xW5p0L0p15_1/sky130_fd_pr__rf_pfet_01v8_aF04W5p00L0p15_2 I1 I2  VH
+ sky130_fd_pr__rf_pfet_01v8_aF04W5p00L0p15
XXCP_1_0/RF_pfet_28xW5p0L0p15_1/sky130_fd_pr__rf_pfet_01v8_aF04W5p00L0p15_3 I1 I2  VH
+ sky130_fd_pr__rf_pfet_01v8_aF04W5p00L0p15
XXCP_1_0/RF_pfet_28xW5p0L0p15_1/sky130_fd_pr__rf_pfet_01v8_aF04W5p00L0p15_4 I1 I2  VH
+ sky130_fd_pr__rf_pfet_01v8_aF04W5p00L0p15
XXCP_1_0/RF_pfet_28xW5p0L0p15_1/sky130_fd_pr__rf_pfet_01v8_aF04W5p00L0p15_5 I1 I2  VH
+ sky130_fd_pr__rf_pfet_01v8_aF04W5p00L0p15
XXCP_1_0/RF_pfet_28xW5p0L0p15_1/sky130_fd_pr__rf_pfet_01v8_aF04W5p00L0p15_6 I1 I2  VH
+ sky130_fd_pr__rf_pfet_01v8_aF04W5p00L0p15
Xsky130_fd_pr__cap_vpp_08p6x07p8_m1m2m3_shieldl1_3 VL VH VL
+ sky130_fd_pr__cap_vpp_08p6x07p8_m1m2m3_shieldl1
C13 I1 VL 29.45fF
C14 I2 VL 45.54fF
C15 VH VL 543.94fF
C16 captuner_complete_2_0/sky130_fd_pr__rf_nfet_01v8_aM04W5p00L0p15_fingered_6/S VL 6.47fF
C17 G4 VL 5.45fF
C18 captuner_complete_2_0/sky130_fd_pr__rf_nfet_01v8_aM04W5p00L0p15_fingered_4/S VL 2.68fF
C19 G3 VL 4.98fF
C20 G2 VL 3.01fF
C21 G1 VL 2.97fF
C22 G0 VL 3.07fF

.ends

**** Instantiate ****

* XU_XCP VDD GND G1 G2 XCP
* XU_CAPTUNE G1 G2 GND VC0 VC1 VC2 VC3 VC4 CAPTUNE

XU_COMPLETE VDD GND G1 G2 VC0 VC1 VC2 VC3 VC4 COMPLETE

.options savecurrents
.tran 1ps 320ns
.control
run
display
plot v(G1)
plot v(G2)
plot @I1[i]
.endc


**** end user architecture code
**.ends
.GLOBAL GND
.end
